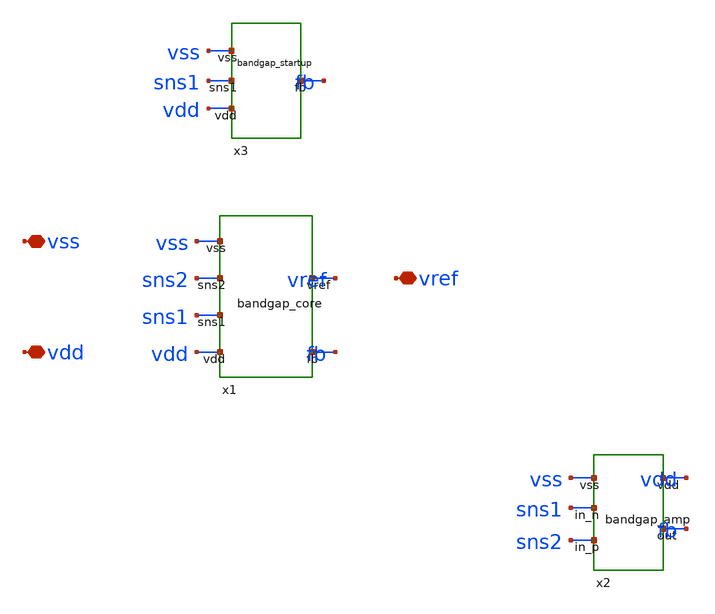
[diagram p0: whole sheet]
** sch_path: design/sg13cmos5l/bandgap_top.sch
**.subckt bandgap_top vdd vss vref
*.iopin vdd
*.iopin vss
*.iopin vref
Xx1 vdd vss fb sns1 sns2 vref bandgap_core
Xx2 sns2 sns1 vss fb vdd bandgap_amp
Xx3 vdd vss sns1 fb bandgap_startup
**.ends

* expanding   symbol:  bandgap_core.sym # of pins=6
** sym_path: design/sg13cmos5l/bandgap_core.sym
** sch_path: design/sg13cmos5l/bandgap_core.sch
.subckt bandgap_core vdd vss fb sns1 sns2 vref

*.iopin vdd
*.iopin vss
*.iopin fb
*.iopin sns1
*.iopin sns2
*.iopin vref
XM1 sns1 fb vdd vdd sg13_hv_pmos w=10u l=1u ng=1 m=1 mm_ok=1
XQ1 vss vss sns1 pnpMPA a=2p p=6u m=1
XM2 sns2 fb vdd vdd sg13_hv_pmos w=10u l=1u ng=1 m=1 mm_ok=1
XR2 sns2 e2 sub! rppd w=2u l=85.1u m=1 b=0 mm_ok=1
XQ2 vss vss e2 pnpMPA a=16p p=20u m=1
XM3 vref fb vdd vdd sg13_hv_pmos w=10u l=1u ng=1 m=1 mm_ok=1
XR1 vref e3 sub! rppd w=2u l=647.0u m=1 b=0 mm_ok=1
XQ3 vss vss e3 pnpMPA a=2p p=6u m=1
.ends


* expanding   symbol:  bandgap_amp.sym # of pins=5
** sym_path: design/sg13cmos5l/bandgap_amp.sym
** sch_path: design/sg13cmos5l/bandgap_amp.sch
.subckt bandgap_amp in_p in_n vss out vdd

*.iopin vdd
*.iopin vss
*.iopin in_p
*.iopin in_n
*.iopin out
XMTAIL tail out vdd vdd sg13_hv_pmos w=10u l=1u ng=1 m=1 mm_ok=1
XMP1 d1 in_p tail vdd sg13_hv_pmos w=20u l=1u ng=1 m=1 mm_ok=1
XMP2 d2 in_n tail vdd sg13_hv_pmos w=20u l=1u ng=1 m=1 mm_ok=1
XMP3 pn pn vdd vdd sg13_hv_pmos w=10u l=1u ng=1 m=1 mm_ok=1
XMP4 out pn vdd vdd sg13_hv_pmos w=10u l=1u ng=1 m=1 mm_ok=1
XMN1 d1 d1 vss vss sg13_hv_nmos w=10u l=1u ng=1 m=1 mm_ok=1
XMN2 d2 d2 vss vss sg13_hv_nmos w=10u l=1u ng=1 m=1 mm_ok=1
XMN3 out d1 vss vss sg13_hv_nmos w=10u l=1u ng=1 m=1 mm_ok=1
XMN4 pn d2 vss vss sg13_hv_nmos w=10u l=1u ng=1 m=1 mm_ok=1
.ends


* expanding   symbol:  bandgap_startup.sym # of pins=4
** sym_path: design/sg13cmos5l/bandgap_startup.sym
** sch_path: design/sg13cmos5l/bandgap_startup.sch
.subckt bandgap_startup vdd vss sns1 fb

*.iopin vdd
*.iopin vss
*.iopin sns1
*.iopin fb
XRPU vdd det sub! rhigh w=1u l=1411.3u m=1 b=0 mm_ok=1
XMSENSE det sns1 vss vss sg13_hv_nmos w=10u l=0.5u ng=1 m=1 mm_ok=1
XMKFB fb det vss vss sg13_hv_nmos w=2u l=0.5u ng=1 m=1 mm_ok=1
.ends

.end
